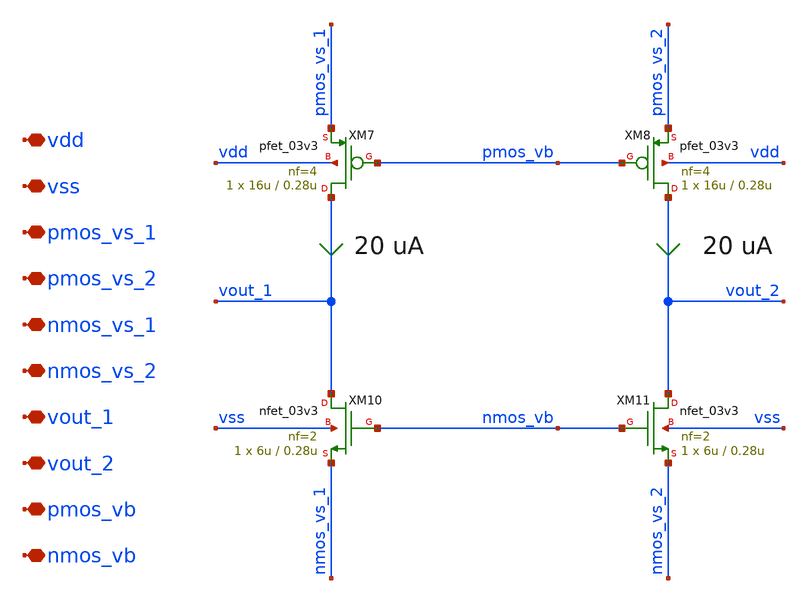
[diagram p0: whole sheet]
** sch_path: xschem/ccia_rrl_ota/b9_ccia_rrl_ota_cascode.sch
**.subckt b9_ccia_rrl_ota_cascode vdd vss pmos_vs_1 pmos_vs_2 nmos_vs_1 nmos_vs_2 vout_1 vout_2
*+ pmos_vb nmos_vb
*.iopin vdd
*.iopin vss
*.iopin pmos_vs_1
*.iopin pmos_vs_2
*.iopin nmos_vs_1
*.iopin nmos_vs_2
*.iopin vout_1
*.iopin vout_2
*.iopin pmos_vb
*.iopin nmos_vb
XM10 vout_1 nmos_vb nmos_vs_1 vss nfet_03v3 L=0.28u W=6u nf=2 ad='int((nf+1)/2) * W/nf * 0.18u' as='int((nf+2)/2) * W/nf * 0.18u'
+ pd='2*int((nf+1)/2) * (W/nf + 0.18u)' ps='2*int((nf+2)/2) * (W/nf + 0.18u)' nrd='0.18u / W' nrs='0.18u / W'
+ sa=0 sb=0 sd=0 m=1
XM11 vout_2 nmos_vb nmos_vs_2 vss nfet_03v3 L=0.28u W=6u nf=2 ad='int((nf+1)/2) * W/nf * 0.18u' as='int((nf+2)/2) * W/nf * 0.18u'
+ pd='2*int((nf+1)/2) * (W/nf + 0.18u)' ps='2*int((nf+2)/2) * (W/nf + 0.18u)' nrd='0.18u / W' nrs='0.18u / W'
+ sa=0 sb=0 sd=0 m=1
XM7 vout_1 pmos_vb pmos_vs_1 vdd pfet_03v3 L=0.28u W=16u nf=4 ad='int((nf+1)/2) * W/nf * 0.18u' as='int((nf+2)/2) * W/nf * 0.18u'
+ pd='2*int((nf+1)/2) * (W/nf + 0.18u)' ps='2*int((nf+2)/2) * (W/nf + 0.18u)' nrd='0.18u / W' nrs='0.18u / W'
+ sa=0 sb=0 sd=0 m=1
XM8 vout_2 pmos_vb pmos_vs_2 vdd pfet_03v3 L=0.28u W=16u nf=4 ad='int((nf+1)/2) * W/nf * 0.18u' as='int((nf+2)/2) * W/nf * 0.18u'
+ pd='2*int((nf+1)/2) * (W/nf + 0.18u)' ps='2*int((nf+2)/2) * (W/nf + 0.18u)' nrd='0.18u / W' nrs='0.18u / W'
+ sa=0 sb=0 sd=0 m=1
**.ends
.end
